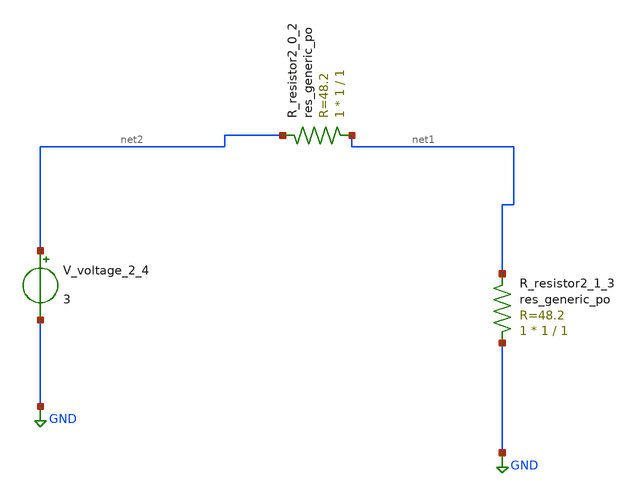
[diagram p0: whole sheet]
** sch_path: schematics/AMSNet/455.sch
**.subckt 455
XR_resistor2_0_2 net1 net2 sky130_fd_pr__res_generic_po W=1 L=1 m=1
XR_resistor2_1_3 GND net1 sky130_fd_pr__res_generic_po W=1 L=1 m=1
V_voltage_2_4 net2 GND 3
**.ends
.GLOBAL GND
.end
